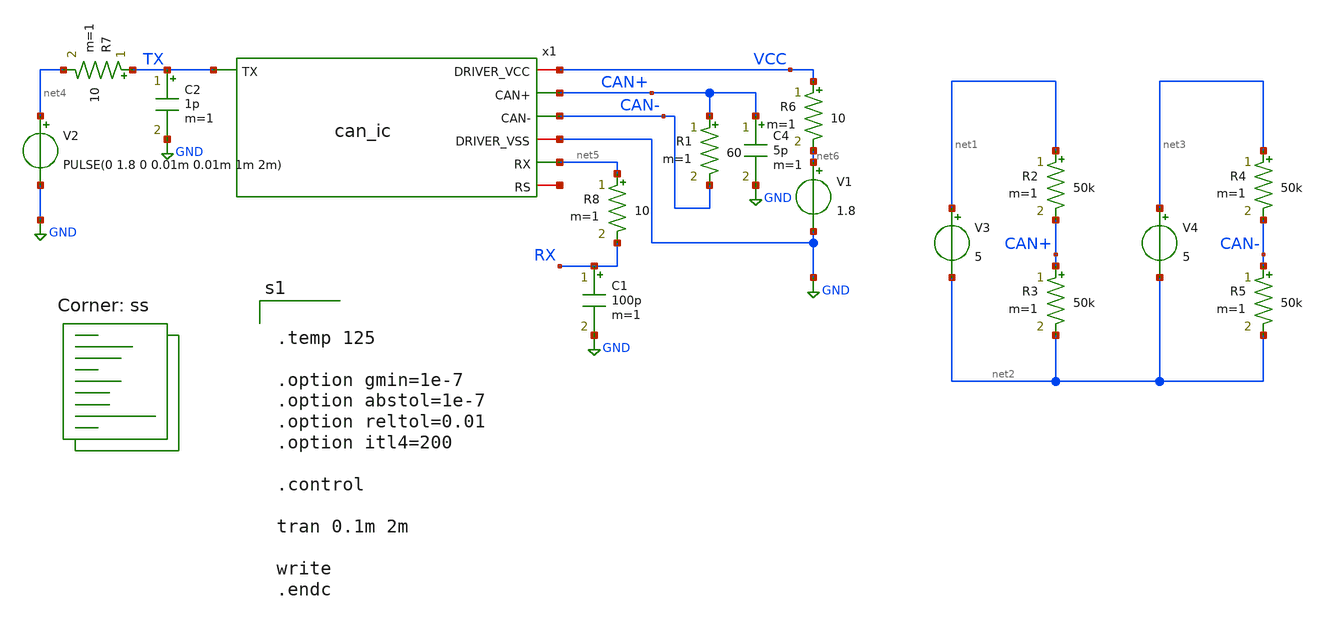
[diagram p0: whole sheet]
** sch_path: ISSCC26/submitted_notebooks/Opensource-ULP-CAN_Transceiver/xschem/can_ic/can_ic_tb.sch
**.subckt can_ic_tb
V1 net6 GND 1.8
R1 CAN+ CAN- 60 m=1
V3 net1 net2 5
R2 net1 CAN+ 50k m=1
R3 CAN+ net2 50k m=1
V4 net3 net2 5
R4 net3 CAN- 50k m=1
R5 CAN- net2 50k m=1
V2 net4 GND PULSE(0 1.8 0 0.01m 0.01m 1m 2m)
R6 VCC net6 10 m=1
R7 TX net4 10 m=1
R8 net5 RX 10 m=1
C1 RX GND 100p m=1
C2 TX GND 1p m=1
C4 CAN+ GND 5p m=1
x1 VCC TX CAN+ CAN- GND net5 net7 can_ic
**** begin user architecture code
.lib $::SKYWATER_MODELS/sky130.lib.spice ss


.temp 125

.option gmin=1e-7
.option abstol=1e-7
.option reltol=0.01
.option itl4=200

.control

tran 0.1m 2m

write
.endc


**** end user architecture code
**.ends

* expanding   symbol:  can_ic.sym # of pins=7
** sym_path: ISSCC26/submitted_notebooks/Opensource-ULP-CAN_Transceiver/xschem/can_ic/can_ic.sym
** sch_path: ISSCC26/submitted_notebooks/Opensource-ULP-CAN_Transceiver/xschem/can_ic/can_ic.sch
.subckt can_ic DRIVER_VCC TX CAN+ CAN- DRIVER_VSS RX RS
*.iopin DRIVER_VCC
*.iopin DRIVER_VSS
*.ipin TX
*.opin CAN+
*.opin CAN-
*.iopin RS
*.opin RX
XM4 CAN- inv_tx DRIVER_VSS DRIVER_VSS sky130_fd_pr__nfet_01v8 W=12 L=0.15 ad='int((1 + 1)/2) * 12 / 1 * 0.29'
+ pd='2*int((1 + 1)/2) * (12 / 1 + 0.29)' as='int((1 + 2)/2) * 12 / 1 * 0.29' ps='2*int((1 + 2)/2) * (12 / 1 + 0.29)'
+ nrd='0.29 / 12 ' nrs='0.29 / 12 ' sa=0 sb=0 sd=0 nf=1 mult=20
XM5 CAN+ TX DRIVER_VCC DRIVER_VCC sky130_fd_pr__pfet_01v8 L=0.15 W=30 nf=1 ad='int((1 + 1)/2) * 30 / 1 * 0.29'
+ as='int((1 + 2)/2) * 30 / 1 * 0.29' pd='2*int((1 + 1)/2) * (30 / 1 + 0.29)' ps='2*int((1 + 2)/2) * (30 / 1 + 0.29)'
+ nrd='0.29 / 30 ' nrs='0.29 / 30 ' sa=0 sb=0 sd=0 mult=20 m=20
XM1 inv_tx TX DRIVER_VSS DRIVER_VSS sky130_fd_pr__nfet_01v8 W=1 L=0.8 ad='int((1 + 1)/2) * 1 / 1 * 0.29'
+ pd='2*int((1 + 1)/2) * (1 / 1 + 0.29)' as='int((1 + 2)/2) * 1 / 1 * 0.29' ps='2*int((1 + 2)/2) * (1 / 1 + 0.29)'
+ nrd='0.29 / 1 ' nrs='0.29 / 1 ' sa=0 sb=0 sd=0 nf=1 mult=4
XM2 net1 net2 DRIVER_VCC DRIVER_VCC sky130_fd_pr__pfet_01v8 L=1 W=2 nf=1 ad='int((nf+1)/2) * W/nf * 0.29'
+ as='int((nf+2)/2) * W/nf * 0.29' pd='2*int((nf+1)/2) * (W/nf + 0.29)' ps='2*int((nf+2)/2) * (W/nf + 0.29)'
+ nrd='0.29 / W' nrs='0.29 / W' sa=0 sb=0 sd=0 mult=2 m=2
XM3 net2 net2 DRIVER_VCC DRIVER_VCC sky130_fd_pr__pfet_01v8 L=1 W=2 nf=1 ad='int((nf+1)/2) * W/nf * 0.29'
+ as='int((nf+2)/2) * W/nf * 0.29' pd='2*int((nf+1)/2) * (W/nf + 0.29)' ps='2*int((nf+2)/2) * (W/nf + 0.29)'
+ nrd='0.29 / W' nrs='0.29 / W' sa=0 sb=0 sd=0 mult=2 m=2
XM6 net1 net1 DRIVER_VSS DRIVER_VSS sky130_fd_pr__nfet_01v8 W=2 L=1 ad='int((nf+1)/2) * W/nf * 0.29'
+ pd='2*int((nf+1)/2) * (W/nf + 0.29)' as='int((nf+2)/2) * W/nf * 0.29' ps='2*int((nf+2)/2) * (W/nf + 0.29)'
+ nrd='0.29 / W' nrs='0.29 / W' sa=0 sb=0 sd=0 nf=1 mult=2
XM7 net2 net1 RS DRIVER_VSS sky130_fd_pr__nfet_01v8 W=2 L=1 ad='int((nf+1)/2) * W/nf * 0.29' pd='2*int((nf+1)/2) * (W/nf + 0.29)'
+ as='int((nf+2)/2) * W/nf * 0.29' ps='2*int((nf+2)/2) * (W/nf + 0.29)' nrd='0.29 / W' nrs='0.29 / W' sa=0
+ sb=0 sd=0 nf=1 mult=2
XM8 net3 net2 DRIVER_VCC DRIVER_VCC sky130_fd_pr__pfet_01v8 L=1 W=2 nf=1 ad='int((nf+1)/2) * W/nf * 0.29'
+ as='int((nf+2)/2) * W/nf * 0.29' pd='2*int((nf+1)/2) * (W/nf + 0.29)' ps='2*int((nf+2)/2) * (W/nf + 0.29)'
+ nrd='0.29 / W' nrs='0.29 / W' sa=0 sb=0 sd=0 mult=2 m=2
XM9 net4 net6 net3 DRIVER_VCC sky130_fd_pr__pfet_01v8 L=0.5 W=1 nf=1 ad='int((nf+1)/2) * W/nf * 0.29'
+ as='int((nf+2)/2) * W/nf * 0.29' pd='2*int((nf+1)/2) * (W/nf + 0.29)' ps='2*int((nf+2)/2) * (W/nf + 0.29)'
+ nrd='0.29 / W' nrs='0.29 / W' sa=0 sb=0 sd=0 mult=4 m=4
XM10 net5 net7 net3 DRIVER_VCC sky130_fd_pr__pfet_01v8 L=0.5 W=1 nf=1 ad='int((nf+1)/2) * W/nf * 0.29'
+ as='int((nf+2)/2) * W/nf * 0.29' pd='2*int((nf+1)/2) * (W/nf + 0.29)' ps='2*int((nf+2)/2) * (W/nf + 0.29)'
+ nrd='0.29 / W' nrs='0.29 / W' sa=0 sb=0 sd=0 mult=4 m=4
XM11 net4 net4 DRIVER_VSS DRIVER_VSS sky130_fd_pr__nfet_01v8 W=1 L=0.8 ad='int((nf+1)/2) * W/nf * 0.29'
+ pd='2*int((nf+1)/2) * (W/nf + 0.29)' as='int((nf+2)/2) * W/nf * 0.29' ps='2*int((nf+2)/2) * (W/nf + 0.29)'
+ nrd='0.29 / W' nrs='0.29 / W' sa=0 sb=0 sd=0 nf=1 mult=4
XM12 net5 net4 DRIVER_VSS DRIVER_VSS sky130_fd_pr__nfet_01v8 W=1 L=0.8 ad='int((nf+1)/2) * W/nf * 0.29'
+ pd='2*int((nf+1)/2) * (W/nf + 0.29)' as='int((nf+2)/2) * W/nf * 0.29' ps='2*int((nf+2)/2) * (W/nf + 0.29)'
+ nrd='0.29 / W' nrs='0.29 / W' sa=0 sb=0 sd=0 nf=1 mult=4
XM13 RX net5 DRIVER_VSS DRIVER_VSS sky130_fd_pr__nfet_01v8 W=4 L=0.8 ad='int((nf+1)/2) * W/nf * 0.29'
+ pd='2*int((nf+1)/2) * (W/nf + 0.29)' as='int((nf+2)/2) * W/nf * 0.29' ps='2*int((nf+2)/2) * (W/nf + 0.29)'
+ nrd='0.29 / W' nrs='0.29 / W' sa=0 sb=0 sd=0 nf=1 mult=4
XR7 inv_tx DRIVER_VCC DRIVER_VCC sky130_fd_pr__res_high_po_1p41 L=40 mult=1 m=1
XR5 net7 CAN- DRIVER_VCC sky130_fd_pr__res_high_po_1p41 L=42 mult=1 m=1
XR1 CAN+ net6 DRIVER_VCC sky130_fd_pr__res_high_po_1p41 L=42 mult=1 m=1
XR3 DRIVER_VCC RX DRIVER_VCC sky130_fd_pr__res_high_po_1p41 L=42 mult=1 m=1
XR4 RX net7 DRIVER_VCC sky130_fd_pr__res_high_po_1p41 L=64 mult=1 m=1
XR2 DRIVER_VCC TX DRIVER_VCC sky130_fd_pr__res_high_po_1p41 L=42 mult=1 m=1
.ends

.GLOBAL GND
.end
